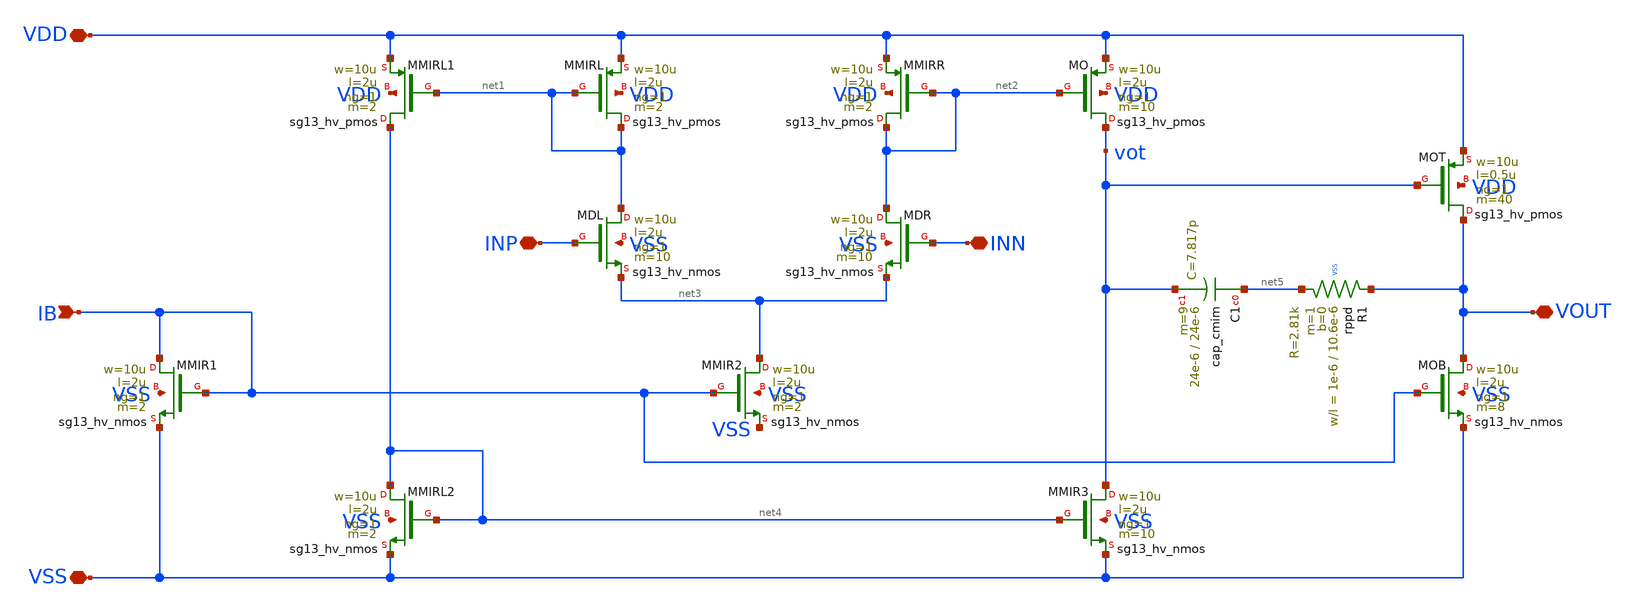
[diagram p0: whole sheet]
** sch_path: ip/ldo/xschem/ldoota.sch
**.subckt ldoota IB VDD VSS INP INN VOUT
*.ipin IB
*.iopin VDD
*.iopin VSS
*.iopin INP
*.iopin INN
*.iopin VOUT
XMMIRL1 net4 net1 VDD VDD sg13_hv_pmos w=10u l=2u ng=1 m=2 mm_ok=1
XMMIRR net2 net2 VDD VDD sg13_hv_pmos w=10u l=2u ng=1 m=2 mm_ok=1
XMMIRL net1 net1 VDD VDD sg13_hv_pmos w=10u l=2u ng=1 m=2 mm_ok=1
XMO vot net2 VDD VDD sg13_hv_pmos w=10u l=2u ng=1 m=10 mm_ok=1
XMOT VOUT vot VDD VDD sg13_hv_pmos w=10u l=0.5u ng=1 m=40 mm_ok=1
XMDL net1 INP net3 VSS sg13_hv_nmos w=10u l=2u ng=1 m=10 mm_ok=1
XMDR net2 INN net3 VSS sg13_hv_nmos w=10u l=2u ng=1 m=10 mm_ok=1
XMMIR2 net3 IB VSS VSS sg13_hv_nmos w=10u l=2u ng=1 m=2 mm_ok=1
XMOB VOUT IB VSS VSS sg13_hv_nmos w=10u l=2u ng=1 m=8 mm_ok=1
XMMIR3 vot net4 VSS VSS sg13_hv_nmos w=10u l=2u ng=1 m=10 mm_ok=1
XMMIRL2 net4 net4 VSS VSS sg13_hv_nmos w=10u l=2u ng=1 m=2 mm_ok=1
XMMIR1 IB IB VSS VSS sg13_hv_nmos w=10u l=2u ng=1 m=2 mm_ok=1
XR1 VOUT net5 VSS rppd w=1e-6 l=10.6e-6 m=1 b=0 mm_ok=1
XC1 net5 vot cap_cmim w=24e-6 l=24e-6 m=9 mm_ok=1
**.ends
.end
